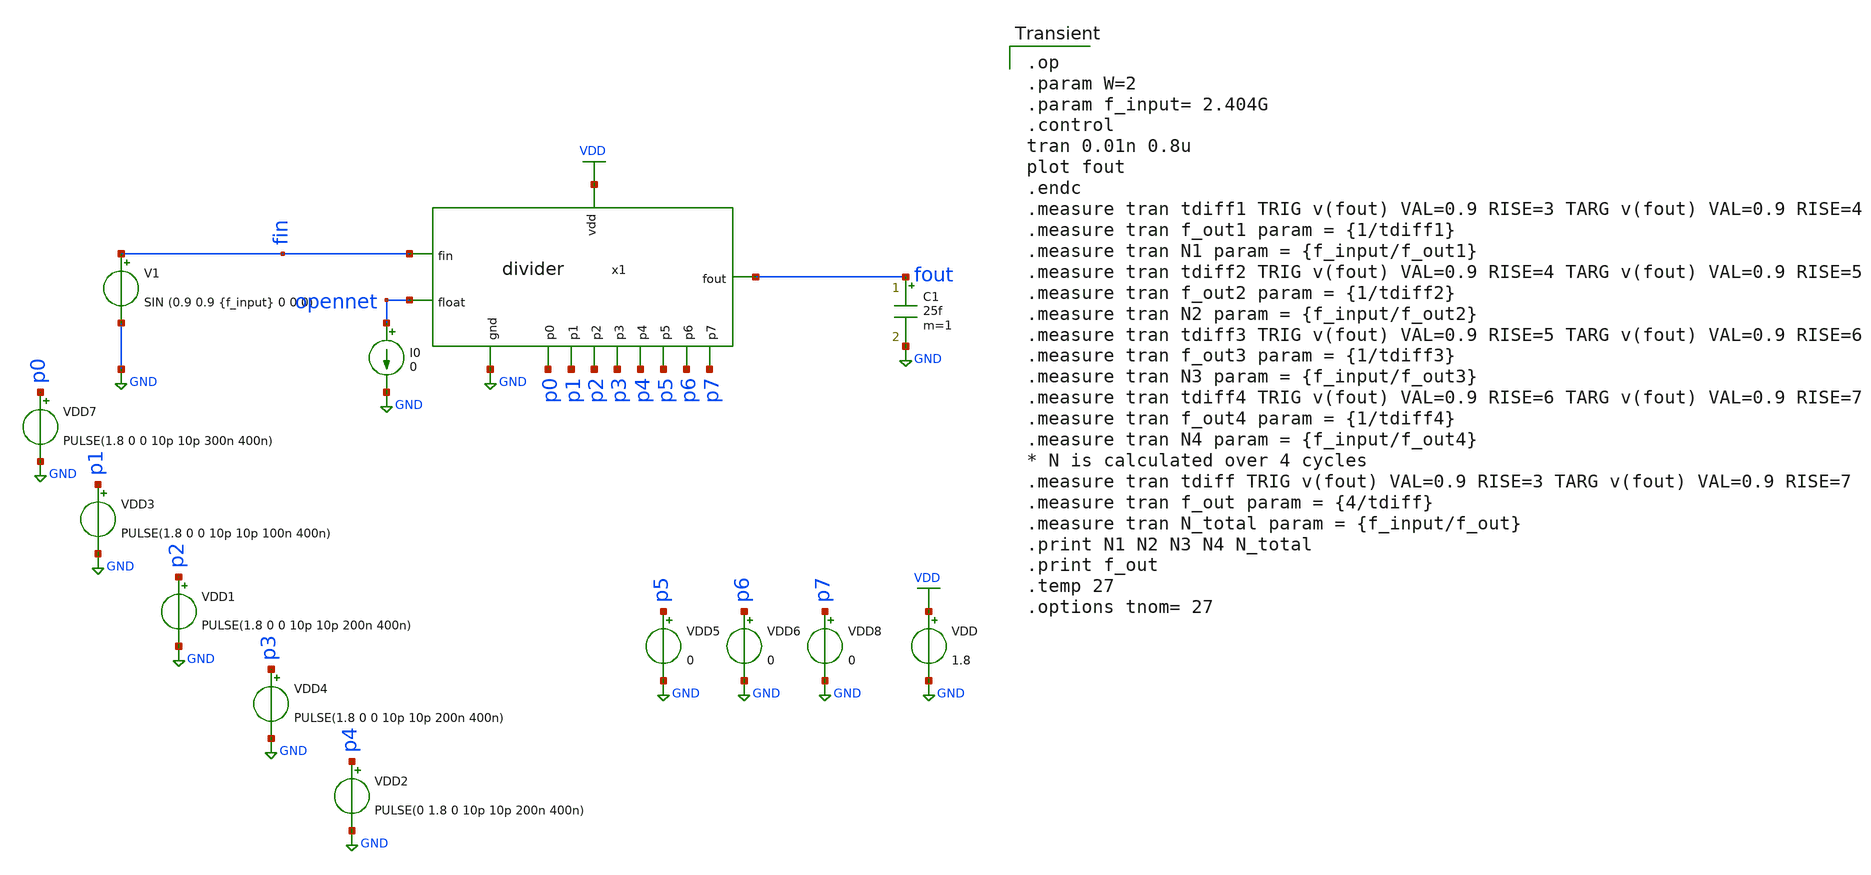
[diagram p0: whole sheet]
** sch_path: pll/dividers_lib/frequency-hopping_testing/xschem/divider_tb_hopping.sch
**.subckt divider_tb_hopping
VDD VDD GND 1.8
VDD5 p5 GND 0
VDD6 p6 GND 0
VDD8 p7 GND 0
x1 VDD fout GND p2 p7 p1 p6 p5 p4 p3 p0 fin opennet divider
V1 fin GND SIN (0.9 0.9 {f_input} 0 0 0)
C1 fout GND 25f m=1
I0 opennet GND 0
VDD1 p2 GND PULSE(1.8 0 0 10p 10p 200n 400n)
VDD2 p4 GND PULSE(0 1.8 0 10p 10p 200n 400n)
VDD3 p1 GND PULSE(1.8 0 0 10p 10p 100n 400n)
VDD4 p3 GND PULSE(1.8 0 0 10p 10p 200n 400n)
VDD7 p0 GND PULSE(1.8 0 0 10p 10p 300n 400n)
**** begin user architecture code

.op
.param W=2
.param f_input= 2.404G
.control
tran 0.01n 0.8u
plot fout
.endc
.measure tran tdiff1 TRIG v(fout) VAL=0.9 RISE=3 TARG v(fout) VAL=0.9 RISE=4
.measure tran f_out1 param = {1/tdiff1}
.measure tran N1 param = {f_input/f_out1}
.measure tran tdiff2 TRIG v(fout) VAL=0.9 RISE=4 TARG v(fout) VAL=0.9 RISE=5
.measure tran f_out2 param = {1/tdiff2}
.measure tran N2 param = {f_input/f_out2}
.measure tran tdiff3 TRIG v(fout) VAL=0.9 RISE=5 TARG v(fout) VAL=0.9 RISE=6
.measure tran f_out3 param = {1/tdiff3}
.measure tran N3 param = {f_input/f_out3}
.measure tran tdiff4 TRIG v(fout) VAL=0.9 RISE=6 TARG v(fout) VAL=0.9 RISE=7
.measure tran f_out4 param = {1/tdiff4}
.measure tran N4 param = {f_input/f_out4}
* N is calculated over 4 cycles
.measure tran tdiff TRIG v(fout) VAL=0.9 RISE=3 TARG v(fout) VAL=0.9 RISE=7
.measure tran f_out param = {4/tdiff}
.measure tran N_total param = {f_input/f_out}
.print N1 N2 N3 N4 N_total
.print f_out
.temp 27
.options tnom= 27


** opencircuitdesign pdks install
.lib $::SKYWATER_MODELS/sky130.lib.spice tt


**** end user architecture code
**.ends
.GLOBAL VDD
.GLOBAL GND
.end
